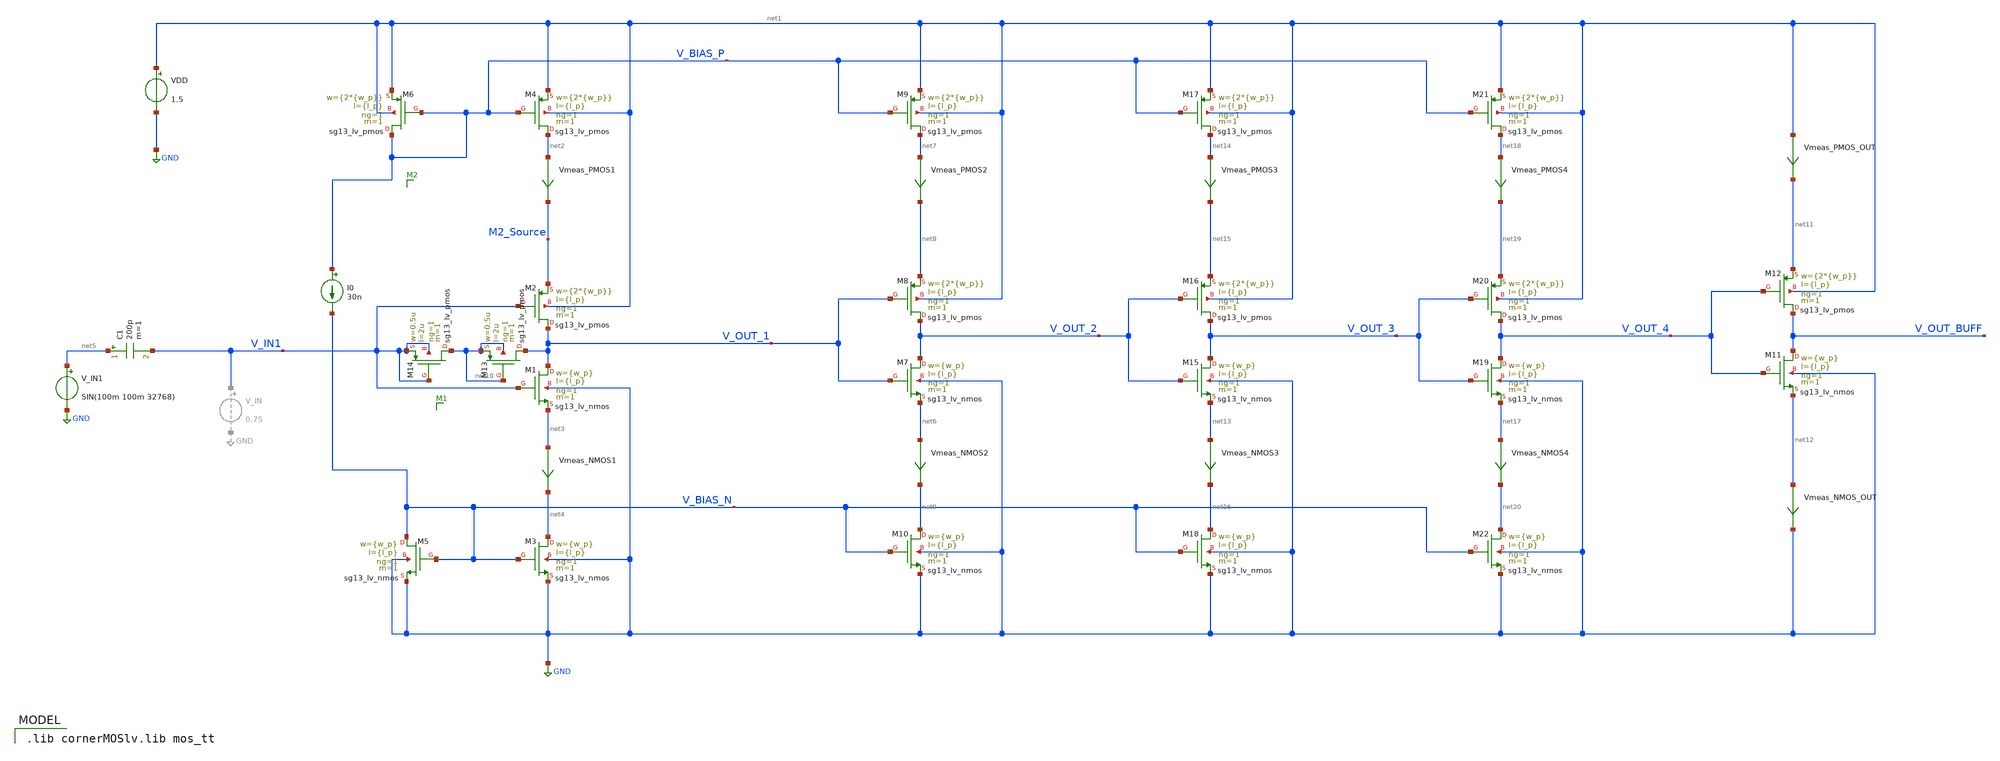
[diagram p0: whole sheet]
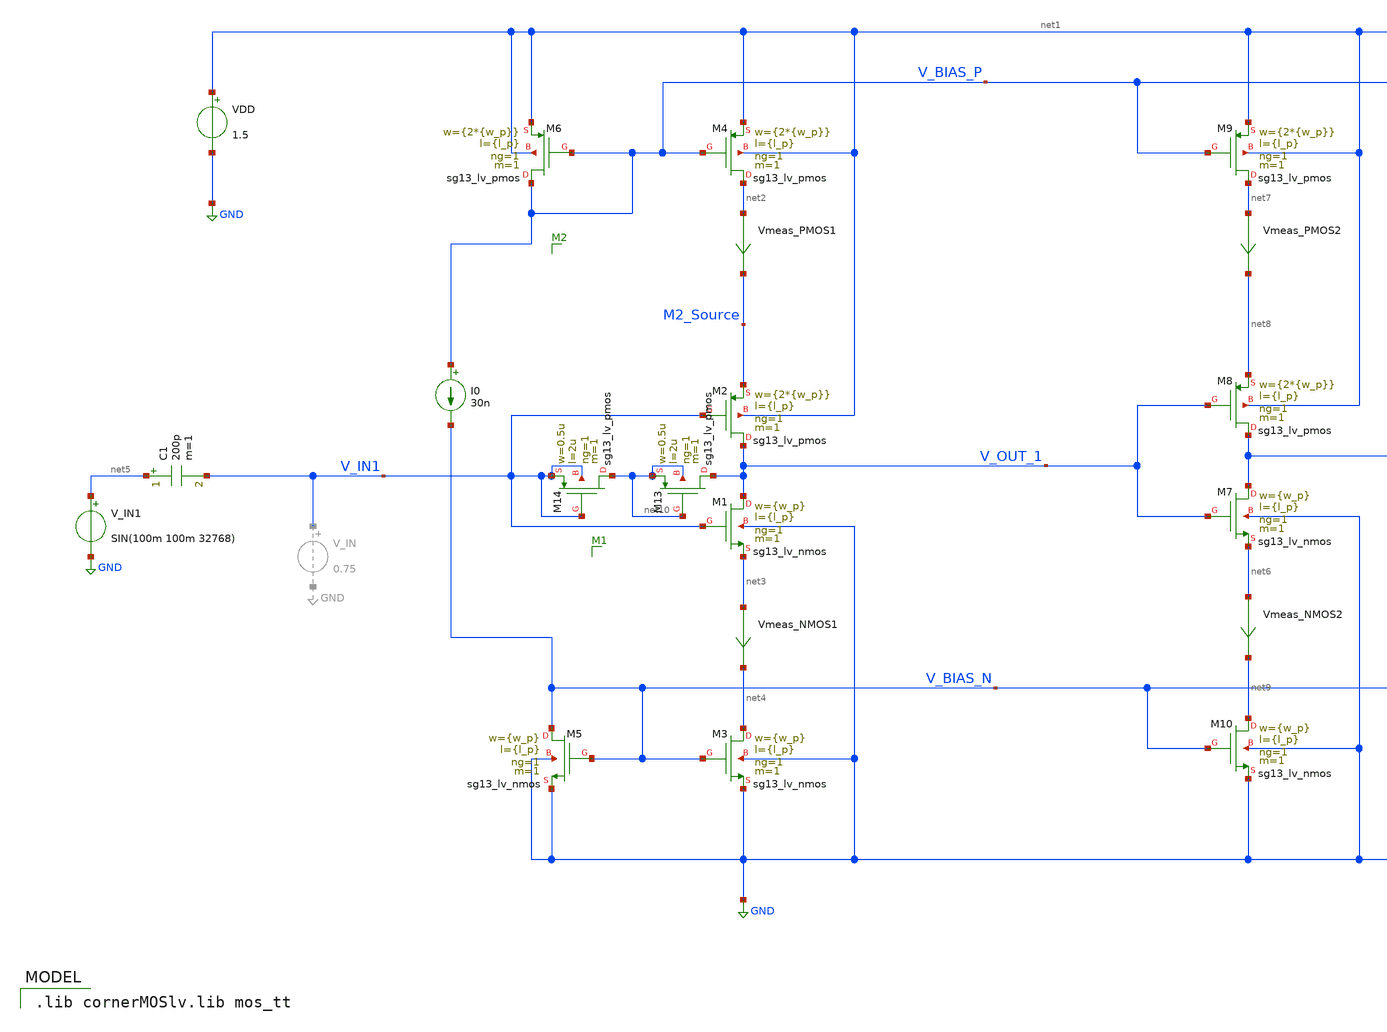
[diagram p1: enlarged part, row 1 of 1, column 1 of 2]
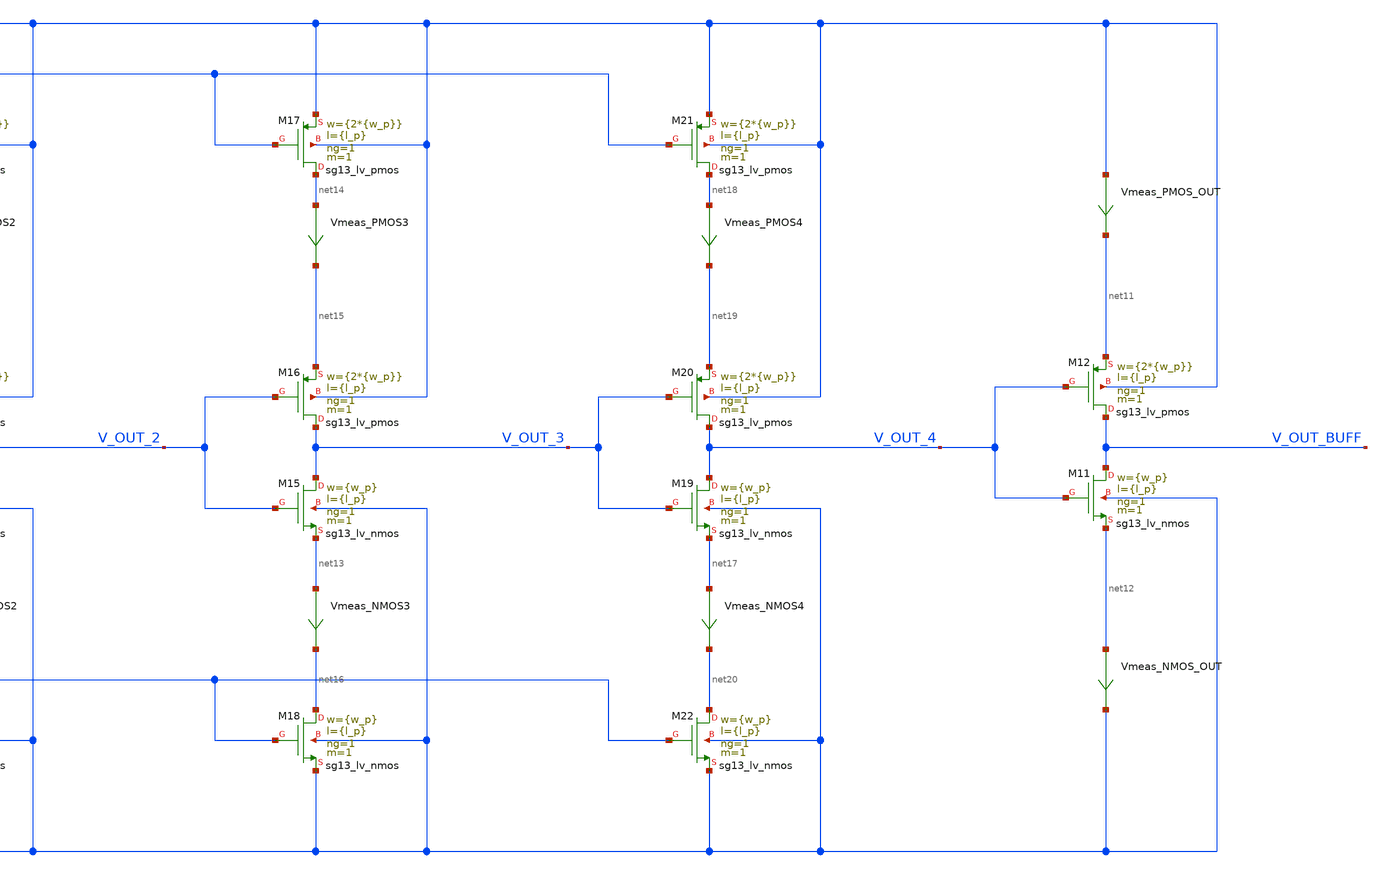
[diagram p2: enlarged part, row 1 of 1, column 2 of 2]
** sch_path: inverter_starved_v1_playground.sch
**.subckt inverter_starved_v1_playground
XM1 V_OUT_1 V_IN1 net3 GND sg13_lv_nmos w={w_p} l={l_p} ng=1 m=1 mm_ok=1
XM2 V_OUT_1 V_IN1 M2_Source net1 sg13_lv_pmos w={2*{w_p}} l={l_p} ng=1 m=1 mm_ok=1
VDD net1 GND 1.5
XM3 net4 V_BIAS_N GND GND sg13_lv_nmos w={w_p} l={l_p} ng=1 m=1 mm_ok=1
XM4 net2 V_BIAS_P net1 net1 sg13_lv_pmos w={2*{w_p}} l={l_p} ng=1 m=1 mm_ok=1
XM5 V_BIAS_N V_BIAS_N GND GND sg13_lv_nmos w={w_p} l={l_p} ng=1 m=1 mm_ok=1
XM6 V_BIAS_P V_BIAS_P net1 net1 sg13_lv_pmos w={2*{w_p}} l={l_p} ng=1 m=1 mm_ok=1
I0 V_BIAS_P V_BIAS_N 30n
Vmeas_PMOS1 net2 M2_Source 0
.save i(vmeas_pmos1)
Vmeas_NMOS1 net3 net4 0
.save i(vmeas_nmos1)
V_IN1 net5 GND SIN(100m 100m 32768)
C1 net5 V_IN1 200p m=1
XM7 V_OUT_2 V_OUT_1 net6 GND sg13_lv_nmos w={w_p} l={l_p} ng=1 m=1 mm_ok=1
XM8 V_OUT_2 V_OUT_1 net8 net1 sg13_lv_pmos w={2*{w_p}} l={l_p} ng=1 m=1 mm_ok=1
Vmeas_NMOS2 net6 net9 0
.save i(vmeas_nmos2)
XM9 net7 V_BIAS_P net1 net1 sg13_lv_pmos w={2*{w_p}} l={l_p} ng=1 m=1 mm_ok=1
Vmeas_PMOS2 net7 net8 0
.save i(vmeas_pmos2)
XM10 net9 V_BIAS_N GND GND sg13_lv_nmos w={w_p} l={l_p} ng=1 m=1 mm_ok=1
XM11 V_OUT_BUFF V_OUT_4 net12 GND sg13_lv_nmos w={w_p} l={l_p} ng=1 m=1 mm_ok=1
XM12 V_OUT_BUFF V_OUT_4 net11 net1 sg13_lv_pmos w={2*{w_p}} l={l_p} ng=1 m=1 mm_ok=1
XM13 V_OUT_1 net10 net10 net10 sg13_lv_pmos w=0.5u l=2u ng=1 m=1 mm_ok=1
XM14 net10 V_IN1 V_IN1 V_IN1 sg13_lv_pmos w=0.5u l=2u ng=1 m=1 mm_ok=1
Vmeas_PMOS_OUT net1 net11 0
.save i(vmeas_pmos_out)
Vmeas_NMOS_OUT net12 GND 0
.save i(vmeas_nmos_out)
XM15 V_OUT_3 V_OUT_2 net13 GND sg13_lv_nmos w={w_p} l={l_p} ng=1 m=1 mm_ok=1
XM16 V_OUT_3 V_OUT_2 net15 net1 sg13_lv_pmos w={2*{w_p}} l={l_p} ng=1 m=1 mm_ok=1
Vmeas_NMOS3 net13 net16 0
.save i(vmeas_nmos3)
XM17 net14 V_BIAS_P net1 net1 sg13_lv_pmos w={2*{w_p}} l={l_p} ng=1 m=1 mm_ok=1
Vmeas_PMOS3 net14 net15 0
.save i(vmeas_pmos3)
XM18 net16 V_BIAS_N GND GND sg13_lv_nmos w={w_p} l={l_p} ng=1 m=1 mm_ok=1
XM19 V_OUT_4 V_OUT_3 net17 GND sg13_lv_nmos w={w_p} l={l_p} ng=1 m=1 mm_ok=1
XM20 V_OUT_4 V_OUT_3 net19 net1 sg13_lv_pmos w={2*{w_p}} l={l_p} ng=1 m=1 mm_ok=1
Vmeas_NMOS4 net17 net20 0
.save i(vmeas_nmos4)
XM21 net18 V_BIAS_P net1 net1 sg13_lv_pmos w={2*{w_p}} l={l_p} ng=1 m=1 mm_ok=1
Vmeas_PMOS4 net18 net19 0
.save i(vmeas_pmos4)
XM22 net20 V_BIAS_N GND GND sg13_lv_nmos w={w_p} l={l_p} ng=1 m=1 mm_ok=1
**** begin user architecture code
 .lib cornerMOSlv.lib mos_tt



.include inverter_starved_playground.save
.param w_p=0.40u l_p=0.13u
.meas tran iavg_stage_1_pmos AVG i(Vmeas_PMOS1)
.meas tran iavg_stage_1_nmos AVG i(Vmeas_NMOS2)
.meas tran iavg_stage_2_pmos AVG i(Vmeas_PMOS2)
.meas tran iavg_stage_2_nmos AVG i(Vmeas_NMOS2)
.meas tran iavg_stage_3_pmos AVG i(Vmeas_PMOS3)
.meas tran iavg_stage_3_nmos AVG i(Vmeas_NMOS3)
.meas tran iavg_stage_4_pmos AVG i(Vmeas_PMOS4)
.meas tran iavg_stage_4_nmos AVG i(Vmeas_NMOS4)
.meas tran iavg_stage_5_pmos AVG i(Vmeas_PMOS_OUT)
.meas tran iavg_stage_5_nmos AVG i(Vmeas_NMOS_OUT)
.meas tran iavg_VDD AVG i(VDD)

.control
save all


tran 0.00001m 0.2m

plot V_IN1 V_OUT_1 V_OUT_2 V_OUT_3 V_OUT_4 V_OUT_BUFF


*fft V_OUT_3
*plot mag(V_OUT_3)

*.measure tran yrms RMS i(VDD) from=0.1m to=0.2m

.endc


**** end user architecture code
**.ends
.GLOBAL GND
.end
